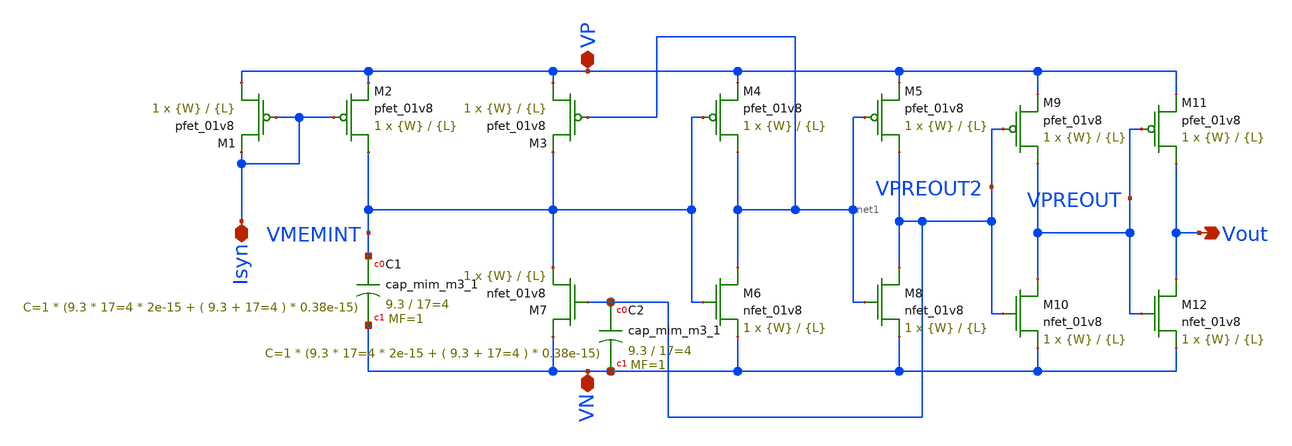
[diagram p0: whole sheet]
** sch_path: schematic/besrour_neuron.sch
**.subckt besrour_neuron VP VN Isyn Vout
*.iopin VP
*.iopin VN
*.iopin Isyn
*.opin Vout
XM1 VP Isyn Isyn VDD sky130_fd_pr__pfet_01v8 L={L} W={W} nf=1 ad='int((nf+1)/2) * W/nf * 0.29' as='int((nf+2)/2) * W/nf * 0.29'
+ pd='2*int((nf+1)/2) * (W/nf + 0.29)' ps='2*int((nf+2)/2) * (W/nf + 0.29)' nrd='0.29 / W' nrs='0.29 / W'
+ sa=0 sb=0 sd=0 mult=1 m=1
XM7 VN VPREOUT2 VMEMINT GND sky130_fd_pr__nfet_01v8 L={L} W={W} nf=1 ad='int((nf+1)/2) * W/nf * 0.29'
+ as='int((nf+2)/2) * W/nf * 0.29' pd='2*int((nf+1)/2) * (W/nf + 0.29)' ps='2*int((nf+2)/2) * (W/nf + 0.29)'
+ nrd='0.29 / W' nrs='0.29 / W' sa=0 sb=0 sd=0 mult=1 m=1
XM2 VMEMINT Isyn VP VDD sky130_fd_pr__pfet_01v8 L={L} W={W} nf=1 ad='int((nf+1)/2) * W/nf * 0.29' as='int((nf+2)/2) * W/nf * 0.29'
+ pd='2*int((nf+1)/2) * (W/nf + 0.29)' ps='2*int((nf+2)/2) * (W/nf + 0.29)' nrd='0.29 / W' nrs='0.29 / W'
+ sa=0 sb=0 sd=0 mult=1 m=1
XM3 VP net1 VMEMINT VDD sky130_fd_pr__pfet_01v8 L={L} W={W} nf=1 ad='int((nf+1)/2) * W/nf * 0.29' as='int((nf+2)/2) * W/nf * 0.29'
+ pd='2*int((nf+1)/2) * (W/nf + 0.29)' ps='2*int((nf+2)/2) * (W/nf + 0.29)' nrd='0.29 / W' nrs='0.29 / W'
+ sa=0 sb=0 sd=0 mult=1 m=1
XM4 net1 VMEMINT VP VDD sky130_fd_pr__pfet_01v8 L={L} W={W} nf=1 ad='int((nf+1)/2) * W/nf * 0.29' as='int((nf+2)/2) * W/nf * 0.29'
+ pd='2*int((nf+1)/2) * (W/nf + 0.29)' ps='2*int((nf+2)/2) * (W/nf + 0.29)' nrd='0.29 / W' nrs='0.29 / W'
+ sa=0 sb=0 sd=0 mult=1 m=1
XM5 VPREOUT2 net1 VP VDD sky130_fd_pr__pfet_01v8 L={L} W={W} nf=1 ad='int((nf+1)/2) * W/nf * 0.29' as='int((nf+2)/2) * W/nf * 0.29'
+ pd='2*int((nf+1)/2) * (W/nf + 0.29)' ps='2*int((nf+2)/2) * (W/nf + 0.29)' nrd='0.29 / W' nrs='0.29 / W'
+ sa=0 sb=0 sd=0 mult=1 m=1
XM6 net1 VMEMINT VN GND sky130_fd_pr__nfet_01v8 L={L} W={W} nf=1 ad='int((nf+1)/2) * W/nf * 0.29' as='int((nf+2)/2) * W/nf * 0.29'
+ pd='2*int((nf+1)/2) * (W/nf + 0.29)' ps='2*int((nf+2)/2) * (W/nf + 0.29)' nrd='0.29 / W' nrs='0.29 / W'
+ sa=0 sb=0 sd=0 mult=1 m=1
XM8 VPREOUT2 net1 VN GND sky130_fd_pr__nfet_01v8 L={L} W={W} nf=1 ad='int((nf+1)/2) * W/nf * 0.29' as='int((nf+2)/2) * W/nf * 0.29'
+ pd='2*int((nf+1)/2) * (W/nf + 0.29)' ps='2*int((nf+2)/2) * (W/nf + 0.29)' nrd='0.29 / W' nrs='0.29 / W'
+ sa=0 sb=0 sd=0 mult=1 m=1
XM9 VPREOUT VPREOUT2 VP VDD sky130_fd_pr__pfet_01v8 L={L} W={W} nf=1 ad='int((nf+1)/2) * W/nf * 0.29'
+ as='int((nf+2)/2) * W/nf * 0.29' pd='2*int((nf+1)/2) * (W/nf + 0.29)' ps='2*int((nf+2)/2) * (W/nf + 0.29)'
+ nrd='0.29 / W' nrs='0.29 / W' sa=0 sb=0 sd=0 mult=1 m=1
XM10 VPREOUT VPREOUT2 VN GND sky130_fd_pr__nfet_01v8 L={L} W={W} nf=1 ad='int((nf+1)/2) * W/nf * 0.29'
+ as='int((nf+2)/2) * W/nf * 0.29' pd='2*int((nf+1)/2) * (W/nf + 0.29)' ps='2*int((nf+2)/2) * (W/nf + 0.29)'
+ nrd='0.29 / W' nrs='0.29 / W' sa=0 sb=0 sd=0 mult=1 m=1
XM11 Vout VPREOUT VP VDD sky130_fd_pr__pfet_01v8 L={L} W={W} nf=1 ad='int((nf+1)/2) * W/nf * 0.29' as='int((nf+2)/2) * W/nf * 0.29'
+ pd='2*int((nf+1)/2) * (W/nf + 0.29)' ps='2*int((nf+2)/2) * (W/nf + 0.29)' nrd='0.29 / W' nrs='0.29 / W'
+ sa=0 sb=0 sd=0 mult=1 m=1
XM12 Vout VPREOUT VN GND sky130_fd_pr__nfet_01v8 L={L} W={W} nf=1 ad='int((nf+1)/2) * W/nf * 0.29' as='int((nf+2)/2) * W/nf * 0.29'
+ pd='2*int((nf+1)/2) * (W/nf + 0.29)' ps='2*int((nf+2)/2) * (W/nf + 0.29)' nrd='0.29 / W' nrs='0.29 / W'
+ sa=0 sb=0 sd=0 mult=1 m=1
XC1 VMEMINT VN sky130_fd_pr__cap_mim_m3_1 W=9.3 L=17=4 MF=1 m=1
XC2 VPREOUT2 VN sky130_fd_pr__cap_mim_m3_1 W=9.3 L=17=4 MF=1 m=1
**.ends
.end
